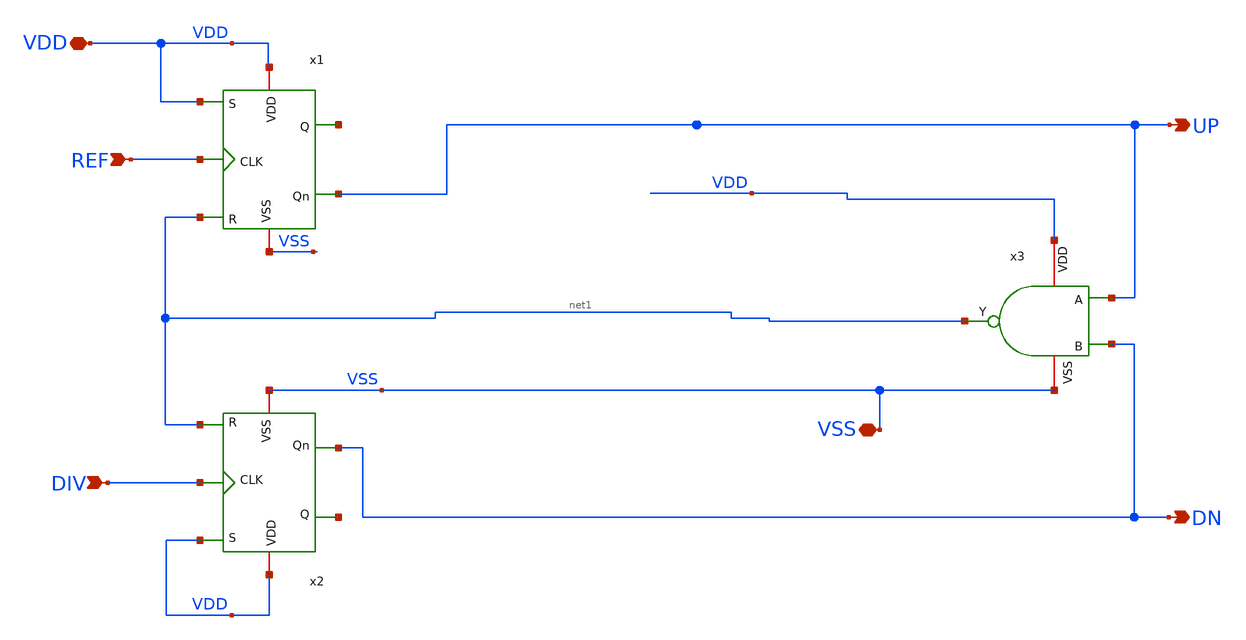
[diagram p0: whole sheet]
** sch_path: src/UN_PFD_GF180mcuD/UN_PFD_UD_GF180mcuD.sch
**.subckt UN_PFD_UD_GF180mcuD VDD VSS REF DIV UP DN
*.iopin VDD
*.iopin VSS
*.ipin REF
*.ipin DIV
*.opin UP
*.opin DN
x3 VDD net1 UP DN VSS UN_NAND2_GF180mcuD
x1 VDD VDD net2 REF VSS UP net1 UN_SRFF_GF180mcuD
x2 VDD VDD net3 DIV VSS DN net1 UN_SRFF_GF180mcuD
**.ends

* expanding   symbol:  /foss/designs/UN_BasicPLL_GF180mcuD/UN_PFD_GF180mcuD/UN_NAND2_GF180mcuD.sym #
*+ of pins=5
** sym_path: src/UN_PFD_GF180mcuD/UN_NAND2_GF180mcuD.sym
** sch_path: src/UN_PFD_GF180mcuD/UN_NAND2_GF180mcuD.sch
.subckt UN_NAND2_GF180mcuD VDD Y A B VSS
*.iopin VDD
*.iopin VSS
*.ipin A
*.ipin B
*.opin Y
XM1 Y A net1 VSS nfet_03v3 L=0.28u W=0.22u nf=1 ad='int((nf+1)/2) * W/nf * 0.18u' as='int((nf+2)/2) * W/nf * 0.18u'
+ pd='2*int((nf+1)/2) * (W/nf + 0.18u)' ps='2*int((nf+2)/2) * (W/nf + 0.18u)' nrd='0.18u / W' nrs='0.18u / W'
+ sa=0 sb=0 sd=0 m=1
XM2 net1 B VSS VSS nfet_03v3 L=0.28u W=0.22u nf=1 ad='int((nf+1)/2) * W/nf * 0.18u' as='int((nf+2)/2) * W/nf * 0.18u'
+ pd='2*int((nf+1)/2) * (W/nf + 0.18u)' ps='2*int((nf+2)/2) * (W/nf + 0.18u)' nrd='0.18u / W' nrs='0.18u / W'
+ sa=0 sb=0 sd=0 m=1
XM3 Y A VDD VDD pfet_03v3 L=0.28u W=0.6u nf=1 ad='int((nf+1)/2) * W/nf * 0.18u' as='int((nf+2)/2) * W/nf * 0.18u'
+ pd='2*int((nf+1)/2) * (W/nf + 0.18u)' ps='2*int((nf+2)/2) * (W/nf + 0.18u)' nrd='0.18u / W' nrs='0.18u / W'
+ sa=0 sb=0 sd=0 m=1
XM4 Y B VDD VDD pfet_03v3 L=0.28u W=0.6u nf=1 ad='int((nf+1)/2) * W/nf * 0.18u' as='int((nf+2)/2) * W/nf * 0.18u'
+ pd='2*int((nf+1)/2) * (W/nf + 0.18u)' ps='2*int((nf+2)/2) * (W/nf + 0.18u)' nrd='0.18u / W' nrs='0.18u / W'
+ sa=0 sb=0 sd=0 m=1
.ends


* expanding   symbol:  /foss/designs/UN_BasicPLL_GF180mcuD/UN_PFD_GF180mcuD/UN_SRFF_GF180mcuD.sym #
*+ of pins=7
** sym_path: src/UN_PFD_GF180mcuD/UN_SRFF_GF180mcuD.sym
** sch_path: src/UN_PFD_GF180mcuD/UN_SRFF_GF180mcuD.sch
.subckt UN_SRFF_GF180mcuD VDD S Q CLK VSS Qn R
*.iopin VDD
*.iopin VSS
*.ipin S
*.ipin R
*.ipin CLK
*.opin Q
*.opin Qn
x1 VDD Q net2 Qn VSS UN_NAND2_GF180mcuD
x2 VDD Qn net1 Q VSS UN_NAND2_GF180mcuD
x3 VDD net2 S CLK VSS UN_NAND2_GF180mcuD
x4 VDD net1 R CLK VSS UN_NAND2_GF180mcuD
.ends

.end
